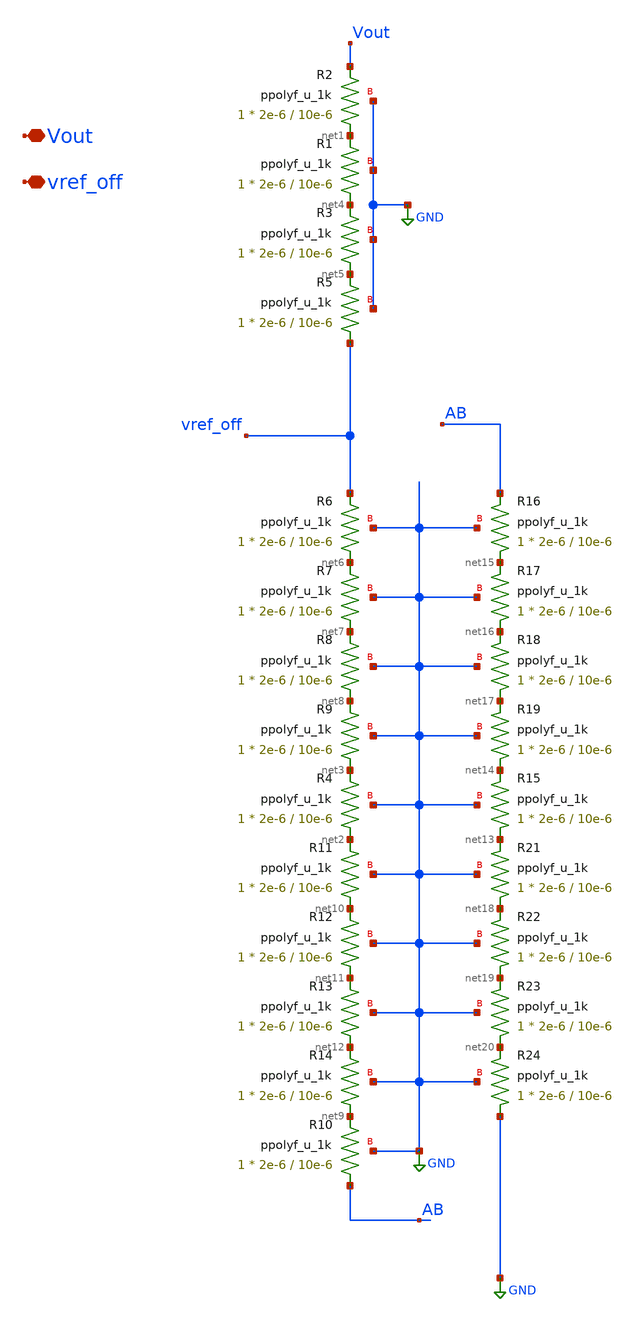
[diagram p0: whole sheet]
** sch_path: Voltage_Reference/LDO/Res_Div.sch
**.subckt Res_Div Vout vref_off
*.iopin Vout
*.iopin vref_off
XR2 net1 Vout GND ppolyf_u_1k r_width=2e-6 r_length=10e-6 m=1
XR4 net2 net3 GND ppolyf_u_1k r_width=2e-6 r_length=10e-6 m=1
XR1 net4 net1 GND ppolyf_u_1k r_width=2e-6 r_length=10e-6 m=1
XR3 net5 net4 GND ppolyf_u_1k r_width=2e-6 r_length=10e-6 m=1
XR5 vref_off net5 GND ppolyf_u_1k r_width=2e-6 r_length=10e-6 m=1
XR6 net6 vref_off GND ppolyf_u_1k r_width=2e-6 r_length=10e-6 m=1
XR7 net7 net6 GND ppolyf_u_1k r_width=2e-6 r_length=10e-6 m=1
XR8 net8 net7 GND ppolyf_u_1k r_width=2e-6 r_length=10e-6 m=1
XR9 net3 net8 GND ppolyf_u_1k r_width=2e-6 r_length=10e-6 m=1
XR10 AB net9 GND ppolyf_u_1k r_width=2e-6 r_length=10e-6 m=1
XR11 net10 net2 GND ppolyf_u_1k r_width=2e-6 r_length=10e-6 m=1
XR12 net11 net10 GND ppolyf_u_1k r_width=2e-6 r_length=10e-6 m=1
XR13 net12 net11 GND ppolyf_u_1k r_width=2e-6 r_length=10e-6 m=1
XR14 net9 net12 GND ppolyf_u_1k r_width=2e-6 r_length=10e-6 m=1
XR15 net13 net14 GND ppolyf_u_1k r_width=2e-6 r_length=10e-6 m=1
XR16 net15 AB GND ppolyf_u_1k r_width=2e-6 r_length=10e-6 m=1
XR17 net16 net15 GND ppolyf_u_1k r_width=2e-6 r_length=10e-6 m=1
XR18 net17 net16 GND ppolyf_u_1k r_width=2e-6 r_length=10e-6 m=1
XR19 net14 net17 GND ppolyf_u_1k r_width=2e-6 r_length=10e-6 m=1
XR21 net18 net13 GND ppolyf_u_1k r_width=2e-6 r_length=10e-6 m=1
XR22 net19 net18 GND ppolyf_u_1k r_width=2e-6 r_length=10e-6 m=1
XR23 net20 net19 GND ppolyf_u_1k r_width=2e-6 r_length=10e-6 m=1
XR24 GND net20 GND ppolyf_u_1k r_width=2e-6 r_length=10e-6 m=1
**.ends
.GLOBAL GND
.end
